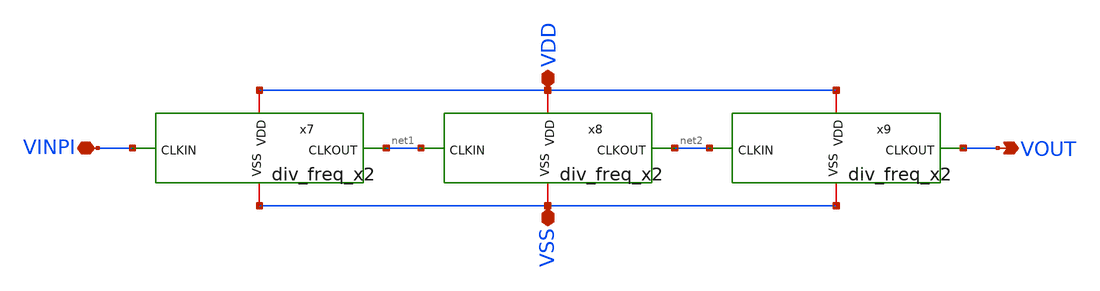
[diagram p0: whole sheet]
** sch_path: Custom_std_cells/div_freq_x8.sch
**.subckt div_freq_x8 VDD VSS VINPI VOUT
*.iopin VDD
*.iopin VSS
*.iopin VINPI
*.opin VOUT
x7 VDD VSS net1 VINPI div_freq_x2
x8 VDD VSS net2 net1 div_freq_x2
x9 VDD VSS VOUT net2 div_freq_x2
**.ends

* expanding   symbol:  /foss/designs/PhaseInterpolator/Custom_std_Cells/div_freq_x2.sym # of pins=4
** sym_path: /foss/designs/PhaseInterpolator/Custom_std_Cells/div_freq_x2.sym
** sch_path: /foss/designs/PhaseInterpolator/Custom_std_Cells/div_freq_x2.sch
.subckt div_freq_x2 VDD VSS CLKOUT CLKIN
*.iopin VDD
*.iopin VSS
*.ipin CLKIN
*.opin CLKOUT
x1 VDD CLKIN CLKOUT net1 VSS reg
x4 VDD net1 CLKOUT VSS inv
.ends


* expanding   symbol:  /foss/designs/PhaseInterpolator/Custom_std_Cells/reg.sym # of pins=5
** sym_path: /foss/designs/PhaseInterpolator/Custom_std_Cells/reg.sym
** sch_path: /foss/designs/PhaseInterpolator/Custom_std_Cells/reg.sch
.subckt reg VDD CLK Q D VSS
*.ipin D
*.opin Q
*.iopin VDD
*.iopin VSS
*.ipin CLK
XM2 X CLK net1 VDD sg13_lv_pmos w=0.15u l=0.13u ng=1 m=1 mm_ok=1
XM1 X CLK_B net2 VSS sg13_lv_nmos w=0.15u l=0.13u ng=1 m=1 mm_ok=1
XM3 net1 D VDD VDD sg13_lv_pmos w=0.15u l=0.13u ng=1 m=1 mm_ok=1
XM4 net2 D VSS VSS sg13_lv_nmos w=0.15u l=0.13u ng=1 m=1 mm_ok=1
XM5 Q CLK_B net3 VDD sg13_lv_pmos w=0.15u l=0.13u ng=1 m=1 mm_ok=1
XM6 Q CLK net4 VSS sg13_lv_nmos w=0.15u l=0.13u ng=1 m=1 mm_ok=1
XM7 net3 X VDD VDD sg13_lv_pmos w=0.15u l=0.13u ng=1 m=1 mm_ok=1
XM8 net4 X VSS VSS sg13_lv_nmos w=0.15u l=0.13u ng=1 m=1 mm_ok=1
x1 VDD CLK_B CLK VSS inv
.ends

.end
